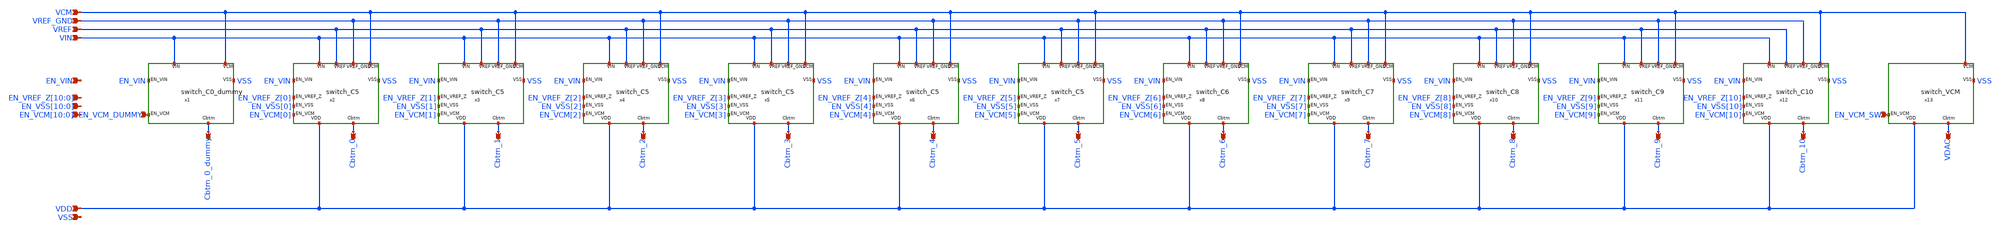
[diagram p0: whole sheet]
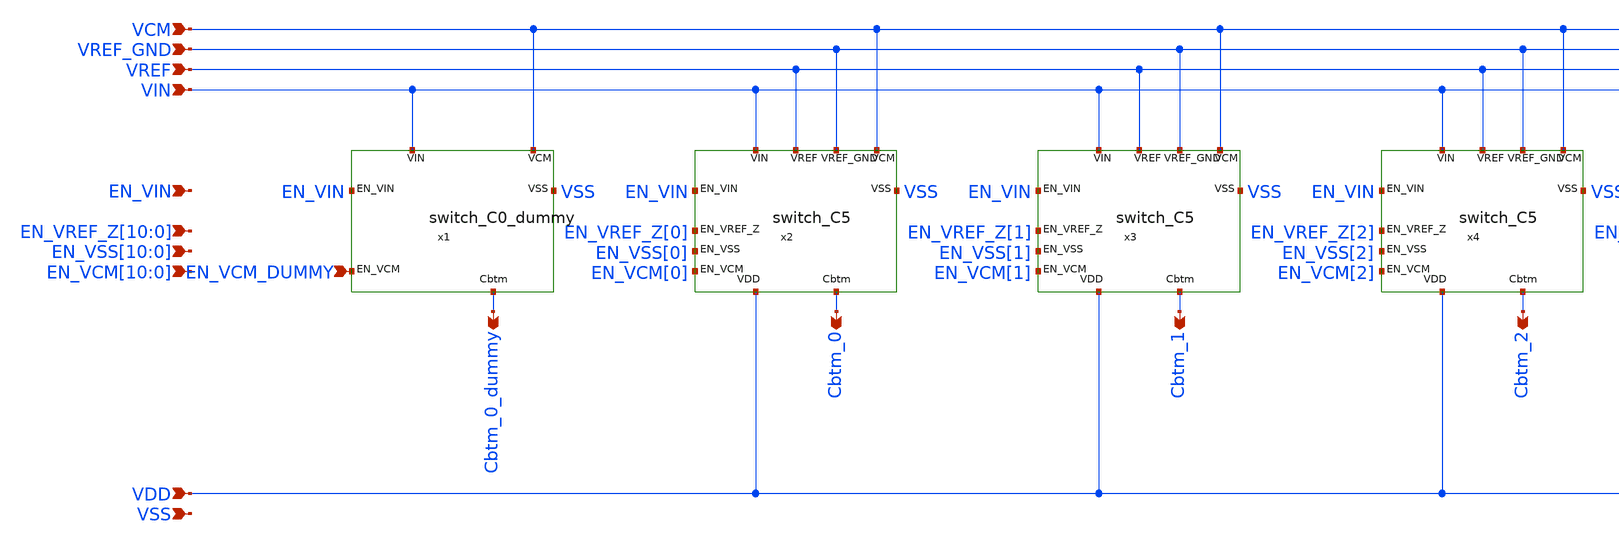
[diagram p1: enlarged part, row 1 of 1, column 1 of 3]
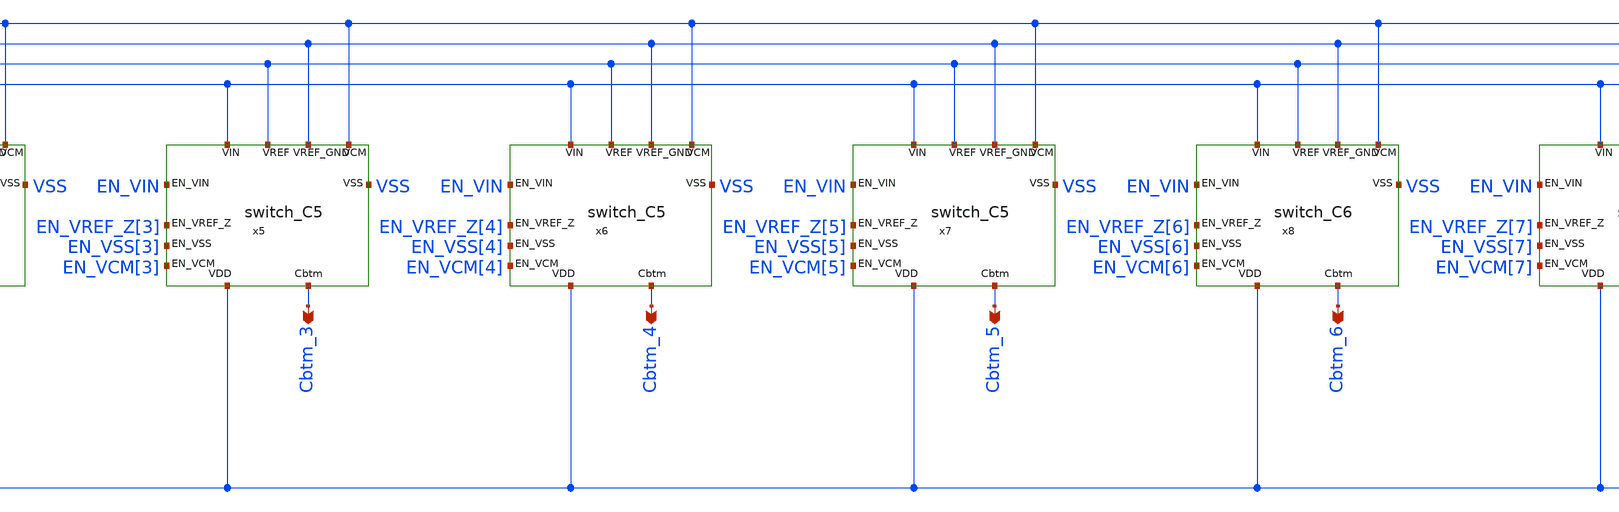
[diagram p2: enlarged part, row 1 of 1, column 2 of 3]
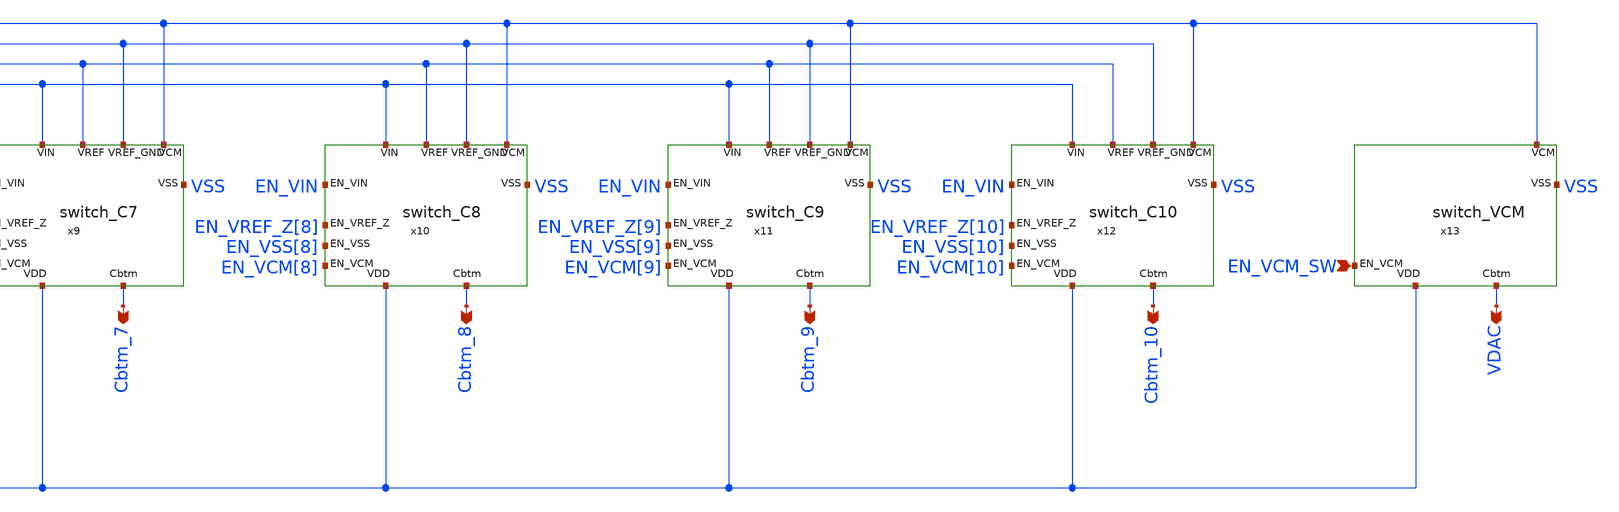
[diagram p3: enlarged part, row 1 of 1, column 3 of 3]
** sch_path: schematic/switches/switches.sch
**.subckt switches VCM VREF_GND VREF VIN VDD Cbtm_0_dummy Cbtm_0 Cbtm_1 Cbtm_2 Cbtm_3 Cbtm_4 Cbtm_5
*+ Cbtm_6 Cbtm_7 Cbtm_8 Cbtm_9 Cbtm_10 VDAC EN_VIN
*+ EN_VREF_Z[10],EN_VREF_Z[9],EN_VREF_Z[8],EN_VREF_Z[7],EN_VREF_Z[6],EN_VREF_Z[5],EN_VREF_Z[4],EN_VREF_Z[3],EN_VREF_Z[2],EN_VREF_Z[1],EN_VREF_Z[0]
*+ EN_VSS[10],EN_VSS[9],EN_VSS[8],EN_VSS[7],EN_VSS[6],EN_VSS[5],EN_VSS[4],EN_VSS[3],EN_VSS[2],EN_VSS[1],EN_VSS[0]
*+ EN_VCM[10],EN_VCM[9],EN_VCM[8],EN_VCM[7],EN_VCM[6],EN_VCM[5],EN_VCM[4],EN_VCM[3],EN_VCM[2],EN_VCM[1],EN_VCM[0] EN_VCM_DUMMY EN_VCM_SW VSS
*.ipin VCM
*.ipin VREF_GND
*.ipin VREF
*.ipin VIN
*.ipin VDD
*.opin Cbtm_0_dummy
*.opin Cbtm_0
*.opin Cbtm_1
*.opin Cbtm_2
*.opin Cbtm_3
*.opin Cbtm_4
*.opin Cbtm_5
*.opin Cbtm_6
*.opin Cbtm_7
*.opin Cbtm_8
*.opin Cbtm_9
*.opin Cbtm_10
*.opin VDAC
*.ipin EN_VIN
*.ipin
*+ EN_VREF_Z[10],EN_VREF_Z[9],EN_VREF_Z[8],EN_VREF_Z[7],EN_VREF_Z[6],EN_VREF_Z[5],EN_VREF_Z[4],EN_VREF_Z[3],EN_VREF_Z[2],EN_VREF_Z[1],EN_VREF_Z[0]
*.ipin
*+ EN_VSS[10],EN_VSS[9],EN_VSS[8],EN_VSS[7],EN_VSS[6],EN_VSS[5],EN_VSS[4],EN_VSS[3],EN_VSS[2],EN_VSS[1],EN_VSS[0]
*.ipin
*+ EN_VCM[10],EN_VCM[9],EN_VCM[8],EN_VCM[7],EN_VCM[6],EN_VCM[5],EN_VCM[4],EN_VCM[3],EN_VCM[2],EN_VCM[1],EN_VCM[0]
*.ipin EN_VCM_DUMMY
*.ipin EN_VCM_SW
*.ipin VSS
x1 VCM VIN EN_VCM_DUMMY Cbtm_0_dummy EN_VIN VSS switch_C0_dummy
x2 VCM VREF_GND VIN VREF EN_VCM[0] EN_VREF_Z[0] Cbtm_0 VDD EN_VSS[0] EN_VIN VSS switch_C5
x3 VCM VREF_GND VIN VREF EN_VCM[1] EN_VREF_Z[1] Cbtm_1 VDD EN_VSS[1] EN_VIN VSS switch_C5
x4 VCM VREF_GND VIN VREF EN_VCM[2] EN_VREF_Z[2] Cbtm_2 VDD EN_VSS[2] EN_VIN VSS switch_C5
x5 VCM VREF_GND VIN VREF EN_VCM[3] EN_VREF_Z[3] Cbtm_3 VDD EN_VSS[3] EN_VIN VSS switch_C5
x6 VCM VREF_GND VIN VREF EN_VCM[4] EN_VREF_Z[4] Cbtm_4 VDD EN_VSS[4] EN_VIN VSS switch_C5
x7 VCM VREF_GND VIN VREF EN_VCM[5] EN_VREF_Z[5] Cbtm_5 VDD EN_VSS[5] EN_VIN VSS switch_C5
x8 VCM VREF_GND VIN VREF EN_VCM[6] EN_VREF_Z[6] Cbtm_6 VDD EN_VSS[6] EN_VIN VSS switch_C6
x9 VCM VREF_GND VIN VREF EN_VCM[7] EN_VREF_Z[7] Cbtm_7 VDD EN_VSS[7] EN_VIN VSS switch_C7
x10 VCM VREF_GND VIN VREF EN_VCM[8] EN_VREF_Z[8] Cbtm_8 VDD EN_VSS[8] EN_VIN VSS switch_C8
x11 VCM VREF_GND VIN VREF EN_VCM[9] EN_VREF_Z[9] Cbtm_9 VDD EN_VSS[9] EN_VIN VSS switch_C9
x12 VCM VREF_GND VIN VREF EN_VCM[10] EN_VREF_Z[10] Cbtm_10 VDD EN_VSS[10] EN_VIN VSS switch_C10
x13 VCM EN_VCM_SW VDAC VDD VSS switch_VCM
**.ends

* expanding   symbol:  individual_switches/switch_C0_dummy.sym # of pins=6
** sym_path: schematic/individual_switches/switch_C0_dummy.sym
** sch_path: schematic/individual_switches/switch_C0_dummy.sch
.subckt switch_C0_dummy VCM VIN EN_VCM Cbtm EN_VIN VSS
*.ipin VIN
*.ipin EN_VIN
*.ipin VCM
*.ipin EN_VCM
*.opin Cbtm
*.iopin VSS
XM7 VIN EN_VIN Cbtm VSS sg13_lv_nmos w=0.55u l=0.13u ng=1 m=1 mm_ok=1
XM1 VCM EN_VCM Cbtm VSS sg13_lv_nmos w=1.15u l=0.13u ng=1 m=1 mm_ok=1
.ends


* expanding   symbol:  individual_switches/switch_C5.sym # of pins=11
** sym_path: schematic/individual_switches/switch_C5.sym
** sch_path: schematic/individual_switches/switch_C5.sch
.subckt switch_C5 VCM VREF_GND VIN VREF EN_VCM EN_VREF_Z Cbtm VDD EN_VSS EN_VIN VSS
*.ipin VIN
*.ipin EN_VIN
*.ipin VREF_GND
*.ipin EN_VSS
*.opin Cbtm
*.iopin VSS
*.ipin VREF
*.ipin EN_VREF_Z
*.ipin EN_VCM
*.ipin VCM
*.iopin VDD
XM7 VIN EN_VIN Cbtm VSS sg13_lv_nmos w=0.55u l=0.13u ng=1 m=1 mm_ok=1
XM1 VCM EN_VCM Cbtm VSS sg13_lv_nmos w=1.15u l=0.13u ng=1 m=1 mm_ok=1
XM2 Cbtm EN_VREF_Z VREF VDD sg13_lv_pmos w=0.35u l=0.35u ng=1 m=1 mm_ok=1
XM4 VREF_GND EN_VSS Cbtm VSS sg13_lv_nmos w=0.88u l=0.13u ng=1 m=1 mm_ok=1
.ends


* expanding   symbol:  individual_switches/switch_C6.sym # of pins=11
** sym_path: schematic/individual_switches/switch_C6.sym
** sch_path: schematic/individual_switches/switch_C6.sch
.subckt switch_C6 VCM VREF_GND VIN VREF EN_VCM EN_VREF_Z Cbtm VDD EN_VSS EN_VIN VSS
*.ipin VIN
*.ipin EN_VIN
*.ipin VREF_GND
*.ipin EN_VSS
*.opin Cbtm
*.iopin VSS
*.ipin VREF
*.ipin EN_VREF_Z
*.ipin EN_VCM
*.ipin VCM
*.iopin VDD
XM7 VIN EN_VIN Cbtm VSS sg13_lv_nmos w=0.55u l=0.13u ng=1 m=1 mm_ok=1
XM1 VREF_GND EN_VSS Cbtm VSS sg13_lv_nmos w=1.75u l=0.13u ng=1 m=1 mm_ok=1
XM2 Cbtm EN_VREF_Z VREF VDD sg13_lv_pmos w=8u l=0.35u ng=1 m=1 mm_ok=1
XM3 VCM EN_VCM Cbtm VSS sg13_lv_nmos w=2.3u l=0.13u ng=1 m=1 mm_ok=1
.ends


* expanding   symbol:  individual_switches/switch_C7.sym # of pins=11
** sym_path: schematic/individual_switches/switch_C7.sym
** sch_path: schematic/individual_switches/switch_C7.sch
.subckt switch_C7 VCM VREF_GND VIN VREF EN_VCM EN_VREF_Z Cbtm VDD EN_VSS EN_VIN VSS
*.ipin VIN
*.ipin EN_VIN
*.ipin VREF_GND
*.ipin EN_VSS
*.opin Cbtm
*.iopin VSS
*.ipin VREF
*.ipin EN_VREF_Z
*.ipin EN_VCM
*.ipin VCM
*.iopin VDD
XM4 VIN EN_VIN Cbtm VSS sg13_lv_nmos w=0.9u l=0.13u ng=1 m=1 mm_ok=1
XM1 VREF_GND EN_VSS Cbtm VSS sg13_lv_nmos w=3.45u l=0.13u ng=1 m=1 mm_ok=1
XM2 Cbtm EN_VREF_Z VREF VDD sg13_lv_pmos w=16u l=0.35u ng=2 m=1 mm_ok=1
XM3 VCM EN_VCM Cbtm VSS sg13_lv_nmos w=4.5u l=0.13u ng=1 m=1 mm_ok=1
.ends


* expanding   symbol:  individual_switches/switch_C8.sym # of pins=11
** sym_path: schematic/individual_switches/switch_C8.sym
** sch_path: schematic/individual_switches/switch_C8.sch
.subckt switch_C8 VCM VREF_GND VIN VREF EN_VCM EN_VREF_Z Cbtm VDD EN_VSS EN_VIN VSS
*.ipin VIN
*.ipin EN_VIN
*.ipin VREF_GND
*.ipin EN_VSS
*.opin Cbtm
*.iopin VSS
*.ipin VREF
*.ipin EN_VREF_Z
*.ipin EN_VCM
*.ipin VCM
*.iopin VDD
XM5 VIN EN_VIN Cbtm VSS sg13_lv_nmos w=0.9u l=0.13u ng=1 m=1 mm_ok=1
XM4 VREF_GND EN_VSS Cbtm VSS sg13_lv_nmos w=6.5u l=0.13u ng=1 m=1 mm_ok=1
XM1 Cbtm EN_VREF_Z VREF VDD sg13_lv_pmos w=32u l=0.35u ng=4 m=1 mm_ok=1
XM2 VCM EN_VCM Cbtm VSS sg13_lv_nmos w=8.5u l=0.13u ng=1 m=1 mm_ok=1
.ends


* expanding   symbol:  individual_switches/switch_C9.sym # of pins=11
** sym_path: schematic/individual_switches/switch_C9.sym
** sch_path: schematic/individual_switches/switch_C9.sch
.subckt switch_C9 VCM VREF_GND VIN VREF EN_VCM EN_VREF_Z Cbtm VDD EN_VSS EN_VIN VSS
*.ipin VIN
*.ipin EN_VIN
*.ipin VREF_GND
*.ipin EN_VSS
*.opin Cbtm
*.iopin VSS
*.ipin VREF
*.ipin EN_VREF_Z
*.ipin EN_VCM
*.ipin VCM
*.iopin VDD
XM3 VIN EN_VIN Cbtm VSS sg13_lv_nmos w=0.9u l=0.13u ng=1 m=1 mm_ok=1
XM5 VREF_GND EN_VSS Cbtm VSS sg13_lv_nmos w=13.1u l=0.13u ng=2 m=1 mm_ok=1
XM1 Cbtm EN_VREF_Z VREF VDD sg13_lv_pmos w=64u l=0.35u ng=8 m=1 mm_ok=1
XM2 VCM EN_VCM Cbtm VSS sg13_lv_nmos w=17u l=0.13u ng=2 m=1 mm_ok=1
.ends


* expanding   symbol:  individual_switches/switch_C10.sym # of pins=11
** sym_path: schematic/individual_switches/switch_C10.sym
** sch_path: schematic/individual_switches/switch_C10.sch
.subckt switch_C10 VCM VREF_GND VIN VREF EN_VCM EN_VREF_Z Cbtm VDD EN_VSS EN_VIN VSS
*.ipin VIN
*.ipin EN_VIN
*.ipin VREF_GND
*.ipin EN_VSS
*.opin Cbtm
*.iopin VSS
*.ipin VREF
*.ipin EN_VREF_Z
*.ipin EN_VCM
*.ipin VCM
*.iopin VDD
XM5 VIN EN_VIN Cbtm VSS sg13_lv_nmos w=6.8u l=0.13u ng=2 m=1 mm_ok=1
XM1 VREF_GND EN_VSS Cbtm VSS sg13_lv_nmos w=26u l=0.13u ng=4 m=1 mm_ok=1
XM2 Cbtm EN_VREF_Z VREF VDD sg13_lv_pmos w=128u l=0.35u ng=16 m=1 mm_ok=1
XM3 VCM EN_VCM Cbtm VSS sg13_lv_nmos w=34u l=0.13u ng=4 m=1 mm_ok=1
.ends


* expanding   symbol:  individual_switches/switch_VCM.sym # of pins=5
** sym_path: schematic/individual_switches/switch_VCM.sym
** sch_path: schematic/individual_switches/switch_VCM.sch
.subckt switch_VCM VCM EN_VCM Cbtm VDD VSS
*.ipin VCM
*.ipin EN_VCM
*.opin Cbtm
*.iopin VSS
*.iopin VDD
XM3 VCM EN_VCM Cbtm VSS sg13_lv_nmos w=34u l=0.13u ng=4 m=1 mm_ok=1
.ends

.end
